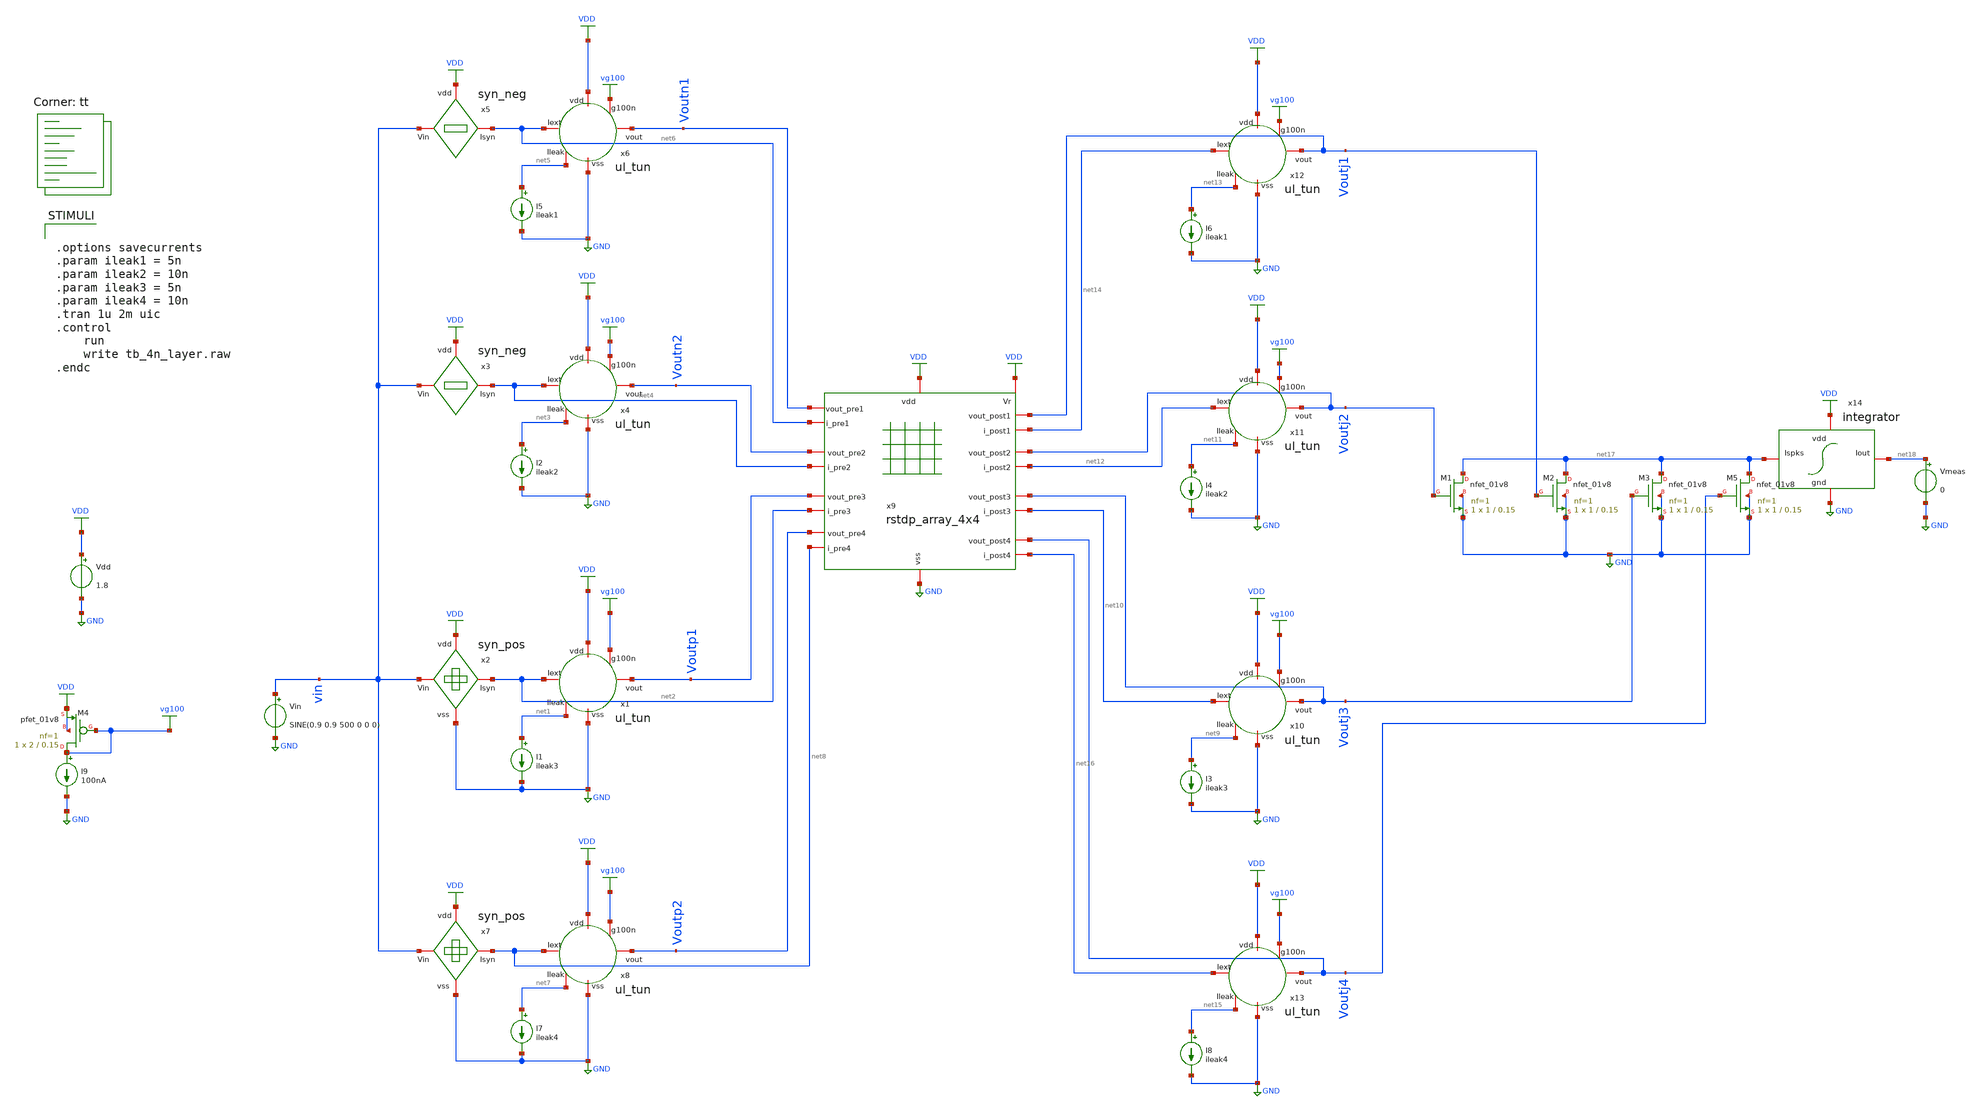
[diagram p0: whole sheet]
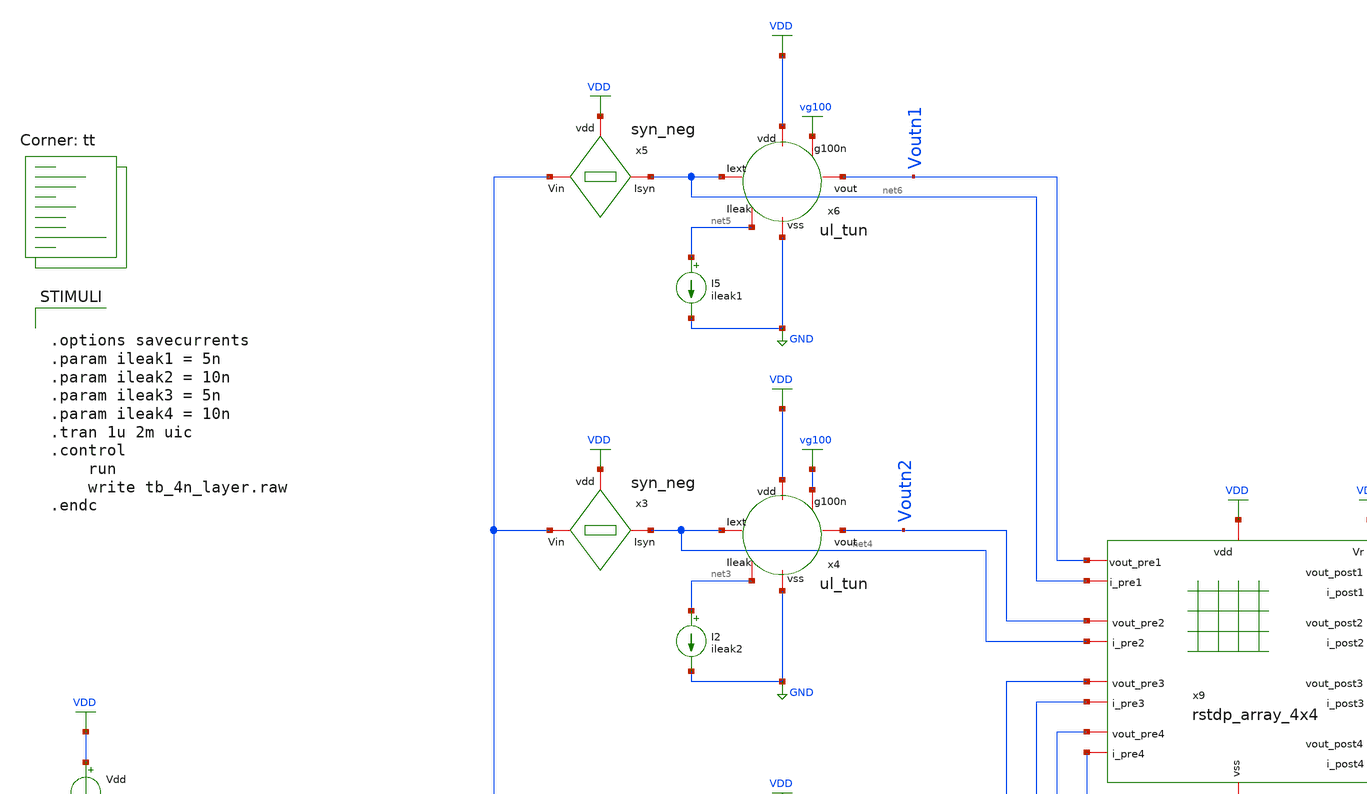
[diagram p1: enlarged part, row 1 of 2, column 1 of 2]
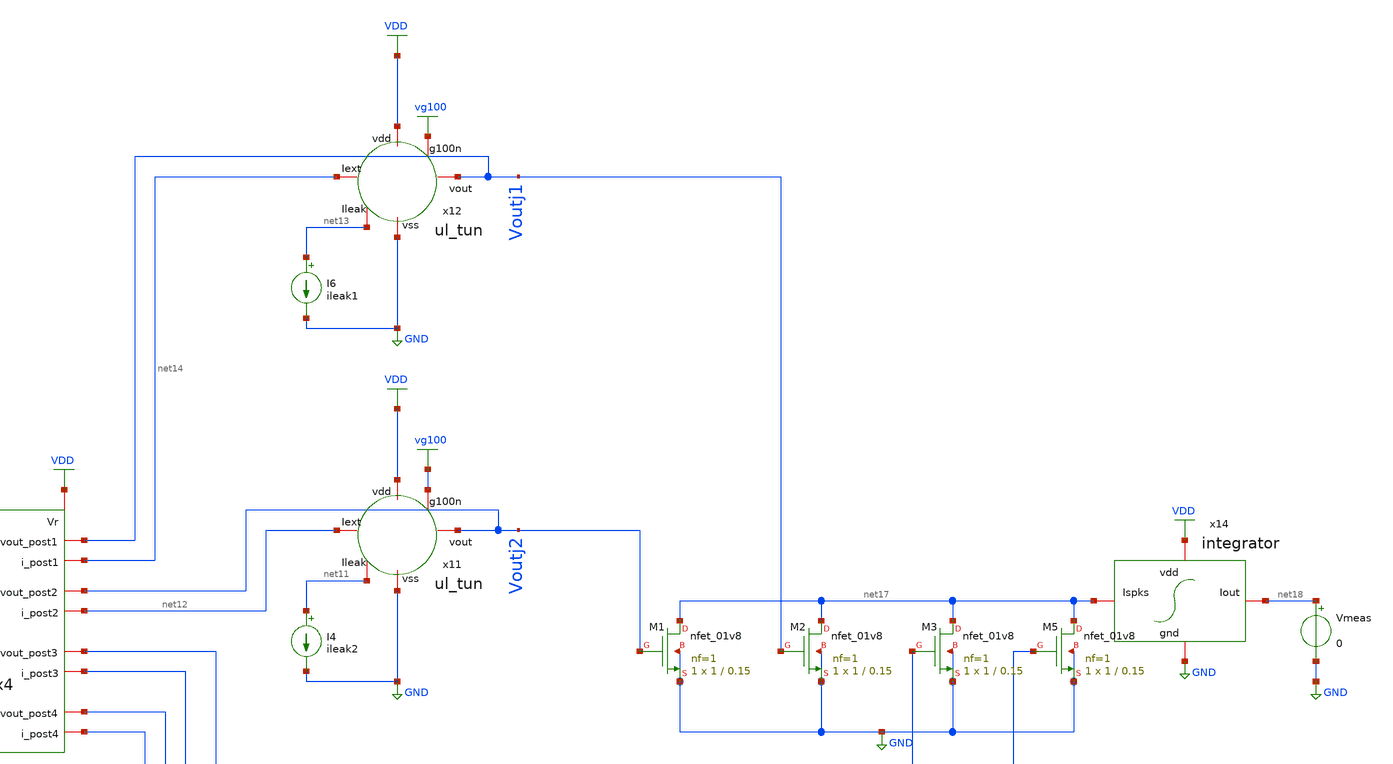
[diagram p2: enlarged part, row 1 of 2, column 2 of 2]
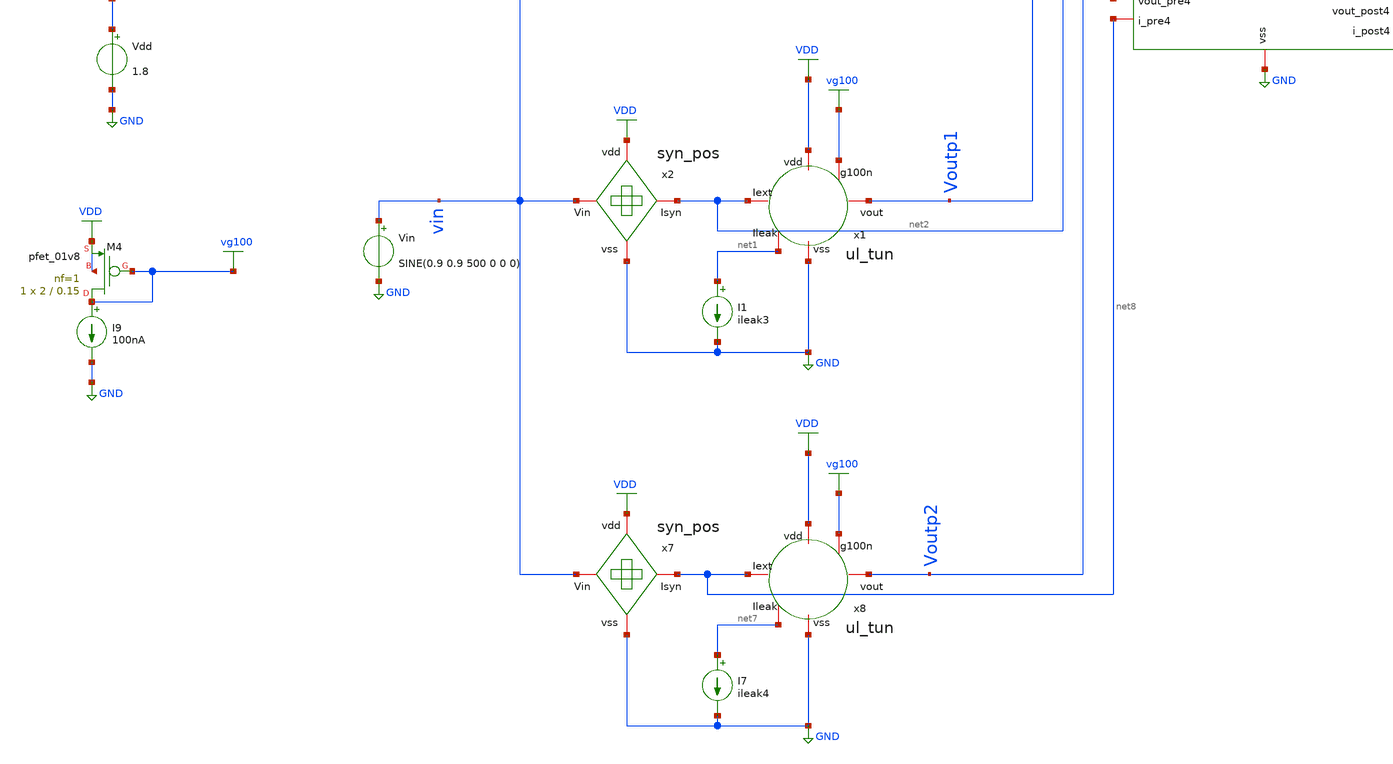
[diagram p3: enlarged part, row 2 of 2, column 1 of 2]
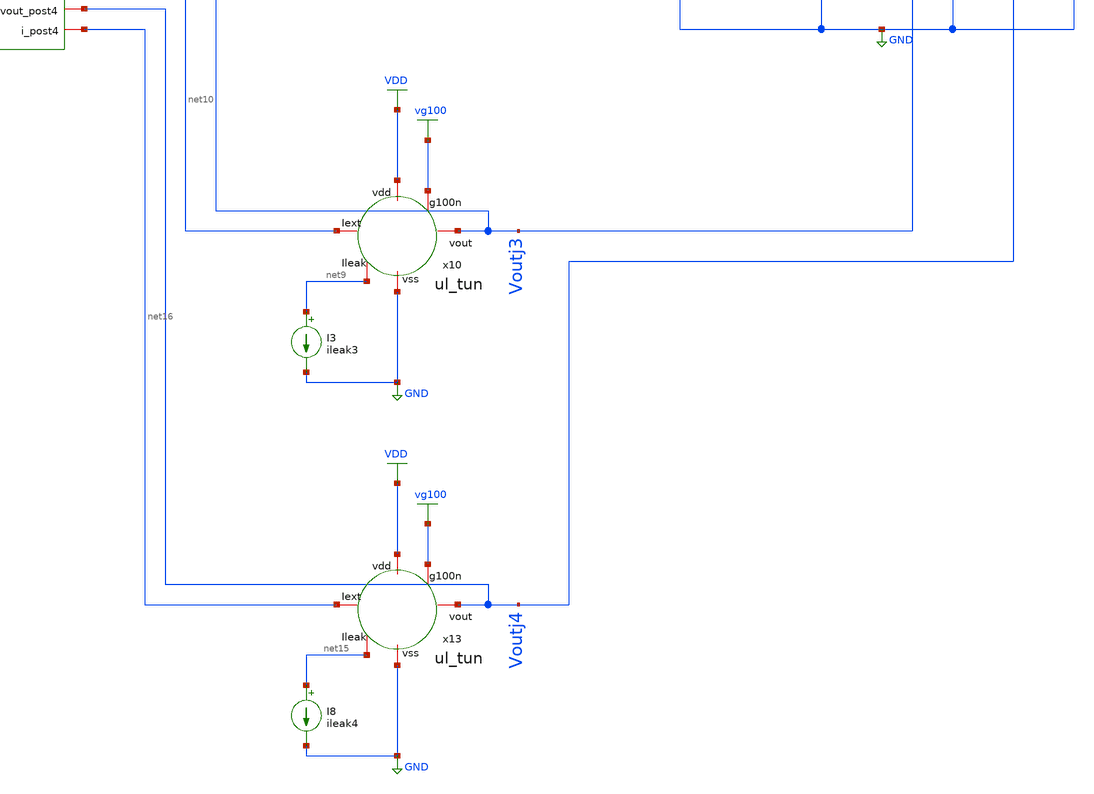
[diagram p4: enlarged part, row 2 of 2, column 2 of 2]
** sch_path: Neuron/ultralif/tb_4n_layer.sch
**.subckt tb_4n_layer
I1 net1 GND ileak3
Vdd VDD GND 1.8
Vin vin GND SINE(0.9 0.9 500 0 0 0)
x2 VDD vin net2 GND syn_pos
x1 net2 VDD vg100 Voutp1 net1 GND ul_tun
I2 net3 GND ileak2
x3 VDD vin net4 syn_neg
x4 net4 VDD vg100 Voutn2 net3 GND ul_tun
I5 net5 GND ileak1
x5 VDD vin net6 syn_neg
x6 net6 VDD vg100 Voutn1 net5 GND ul_tun
I7 net7 GND ileak4
x7 VDD vin net8 GND syn_pos
x8 net8 VDD vg100 Voutp2 net7 GND ul_tun
I9 vg100 GND 100nA
XM4 vg100 vg100 VDD VDD sky130_fd_pr__pfet_01v8 L=0.15 W=2 nf=1 ad='int((nf+1)/2) * W/nf * 0.29' as='int((nf+2)/2) * W/nf * 0.29'
+ pd='2*int((nf+1)/2) * (W/nf + 0.29)' ps='2*int((nf+2)/2) * (W/nf + 0.29)' nrd='0.29 / W' nrs='0.29 / W'
+ sa=0 sb=0 sd=0 mult=1 m=1
x9 VDD VDD net12 net14 Voutj2 net10 GND Voutj1 Voutj3 net16 Voutj4 Voutn1 net6 Voutn2 net4 Voutp1
+ net2 Voutp2 net8 rstdp_array_4x4
I3 net9 GND ileak3
x10 net10 VDD vg100 Voutj3 net9 GND ul_tun
I4 net11 GND ileak2
x11 net12 VDD vg100 Voutj2 net11 GND ul_tun
I6 net13 GND ileak1
x12 net14 VDD vg100 Voutj1 net13 GND ul_tun
I8 net15 GND ileak4
x13 net16 VDD vg100 Voutj4 net15 GND ul_tun
x14 VDD net18 net17 GND integrator
XM1 net17 Voutj2 GND GND sky130_fd_pr__nfet_01v8 L=0.15 W=1 nf=1 ad='int((nf+1)/2) * W/nf * 0.29' as='int((nf+2)/2) * W/nf * 0.29'
+ pd='2*int((nf+1)/2) * (W/nf + 0.29)' ps='2*int((nf+2)/2) * (W/nf + 0.29)' nrd='0.29 / W' nrs='0.29 / W'
+ sa=0 sb=0 sd=0 mult=1 m=1
XM2 net17 Voutj1 GND GND sky130_fd_pr__nfet_01v8 L=0.15 W=1 nf=1 ad='int((nf+1)/2) * W/nf * 0.29' as='int((nf+2)/2) * W/nf * 0.29'
+ pd='2*int((nf+1)/2) * (W/nf + 0.29)' ps='2*int((nf+2)/2) * (W/nf + 0.29)' nrd='0.29 / W' nrs='0.29 / W'
+ sa=0 sb=0 sd=0 mult=1 m=1
XM3 net17 Voutj3 GND GND sky130_fd_pr__nfet_01v8 L=0.15 W=1 nf=1 ad='int((nf+1)/2) * W/nf * 0.29' as='int((nf+2)/2) * W/nf * 0.29'
+ pd='2*int((nf+1)/2) * (W/nf + 0.29)' ps='2*int((nf+2)/2) * (W/nf + 0.29)' nrd='0.29 / W' nrs='0.29 / W'
+ sa=0 sb=0 sd=0 mult=1 m=1
XM5 net17 Voutj4 GND GND sky130_fd_pr__nfet_01v8 L=0.15 W=1 nf=1 ad='int((nf+1)/2) * W/nf * 0.29' as='int((nf+2)/2) * W/nf * 0.29'
+ pd='2*int((nf+1)/2) * (W/nf + 0.29)' ps='2*int((nf+2)/2) * (W/nf + 0.29)' nrd='0.29 / W' nrs='0.29 / W'
+ sa=0 sb=0 sd=0 mult=1 m=1
Vmeas net18 GND 0
**** begin user architecture code
.lib $::SKYWATER_MODELS/sky130.lib.spice tt
**** end user architecture code
**.ends
.GLOBAL GND
.GLOBAL VDD
.GLOBAL vg100
**** begin user architecture code


.options savecurrents
.param ileak1 = 5n
.param ileak2 = 10n
.param ileak3 = 5n
.param ileak4 = 10n
.tran 1u 2m uic
.control
	run
	write tb_4n_layer.raw
.endc


**** end user architecture code
.end
